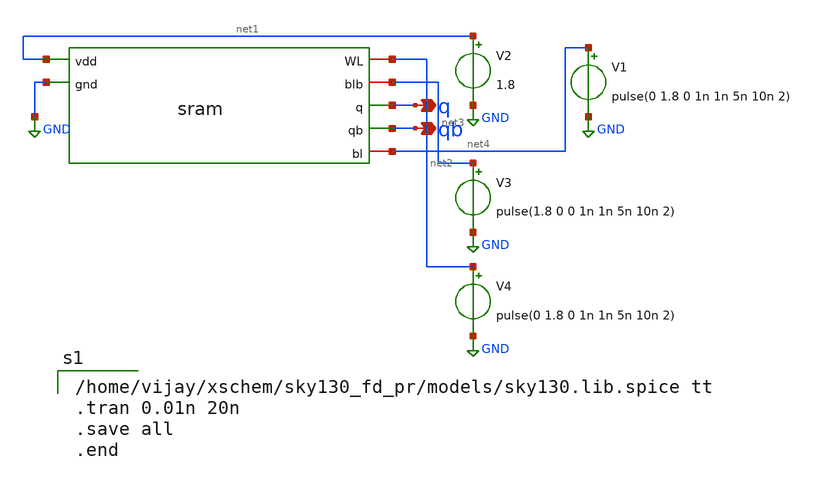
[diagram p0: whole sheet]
** sch_path: untitled-1.sch
**.subckt untitled-1 q qb
*.opin q
*.opin qb
x1 net1 net2 net3 q qb net4 GND sram
V1 net4 GND pulse(0 1.8 0 1n 1n 5n 10n 2)
V2 net1 GND 1.8
V3 net3 GND pulse(1.8 0 0 1n 1n 5n 10n 2)
V4 net2 GND pulse(0 1.8 0 1n 1n 5n 10n 2)
**** begin user architecture code

/home/vijay/xschem/sky130_fd_pr/models/sky130.lib.spice tt
.tran 0.01n 20n
.save all
.end

**** end user architecture code
**.ends

* expanding   symbol:  sram.sym # of pins=7
** sym_path: sram.sym
** sch_path: sram.sch
.subckt sram vdd WL blb q qb bl gnd
*.ipin vdd
*.iopin bl
*.opin q
*.ipin gnd
*.iopin WL
*.iopin blb
*.opin qb
XM1 q qb gnd gnd sky130_fd_pr__nfet_01v8 L=0.15 W=1 nf=1 ad='int((nf+1)/2) * W/nf * 0.29' as='int((nf+2)/2) * W/nf * 0.29'
+ pd='2*int((nf+1)/2) * (W/nf + 0.29)' ps='2*int((nf+2)/2) * (W/nf + 0.29)' nrd='0.29 / W' nrs='0.29 / W'
+ sa=0 sb=0 sd=0 mult=1 m=1
XM2 qb q gnd gnd sky130_fd_pr__nfet_01v8 L=0.15 W=1 nf=1 ad='int((nf+1)/2) * W/nf * 0.29' as='int((nf+2)/2) * W/nf * 0.29'
+ pd='2*int((nf+1)/2) * (W/nf + 0.29)' ps='2*int((nf+2)/2) * (W/nf + 0.29)' nrd='0.29 / W' nrs='0.29 / W'
+ sa=0 sb=0 sd=0 mult=1 m=1
XM3 q WL bl gnd sky130_fd_pr__nfet_01v8 L=0.15 W=1 nf=1 ad='int((nf+1)/2) * W/nf * 0.29' as='int((nf+2)/2) * W/nf * 0.29'
+ pd='2*int((nf+1)/2) * (W/nf + 0.29)' ps='2*int((nf+2)/2) * (W/nf + 0.29)' nrd='0.29 / W' nrs='0.29 / W'
+ sa=0 sb=0 sd=0 mult=1 m=1
XM4 qb WL blb gnd sky130_fd_pr__nfet_01v8 L=0.15 W=1 nf=1 ad='int((nf+1)/2) * W/nf * 0.29' as='int((nf+2)/2) * W/nf * 0.29'
+ pd='2*int((nf+1)/2) * (W/nf + 0.29)' ps='2*int((nf+2)/2) * (W/nf + 0.29)' nrd='0.29 / W' nrs='0.29 / W'
+ sa=0 sb=0 sd=0 mult=1 m=1
XM5 qb q vdd vdd sky130_fd_pr__pfet_01v8_lvt L=0.35 W=1 nf=1 ad='int((nf+1)/2) * W/nf * 0.29' as='int((nf+2)/2) * W/nf * 0.29'
+ pd='2*int((nf+1)/2) * (W/nf + 0.29)' ps='2*int((nf+2)/2) * (W/nf + 0.29)' nrd='0.29 / W' nrs='0.29 / W'
+ sa=0 sb=0 sd=0 mult=1 m=1
XM6 q qb vdd vdd sky130_fd_pr__pfet_01v8_lvt L=0.35 W=1 nf=1 ad='int((nf+1)/2) * W/nf * 0.29' as='int((nf+2)/2) * W/nf * 0.29'
+ pd='2*int((nf+1)/2) * (W/nf + 0.29)' ps='2*int((nf+2)/2) * (W/nf + 0.29)' nrd='0.29 / W' nrs='0.29 / W'
+ sa=0 sb=0 sd=0 mult=1 m=1
.ends

.GLOBAL GND
.end
